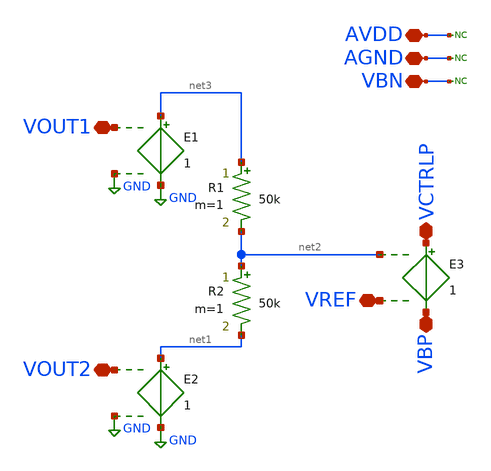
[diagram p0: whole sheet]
** sch_path: ITI_Labs/Lab11_Xschem/Design/CMFB_Behav.sch
**.subckt CMFB_Behav VOUT1 VOUT2 VREF VCTRLP VBP AVDD AGND VBN
*.iopin VOUT1
*.iopin VOUT2
*.iopin VREF
*.iopin VCTRLP
*.iopin VBP
*.iopin AVDD
*.iopin AGND
*.iopin VBN
E1 net3 GND VOUT1 GND 1
E2 net1 GND VOUT2 GND 1
E3 VCTRLP VBP net2 VREF 1
R1 net3 net2 50k m=1
R2 net2 net1 50k m=1
* noconn AVDD
* noconn AGND
* noconn VBN
**.ends
.GLOBAL GND
.end
